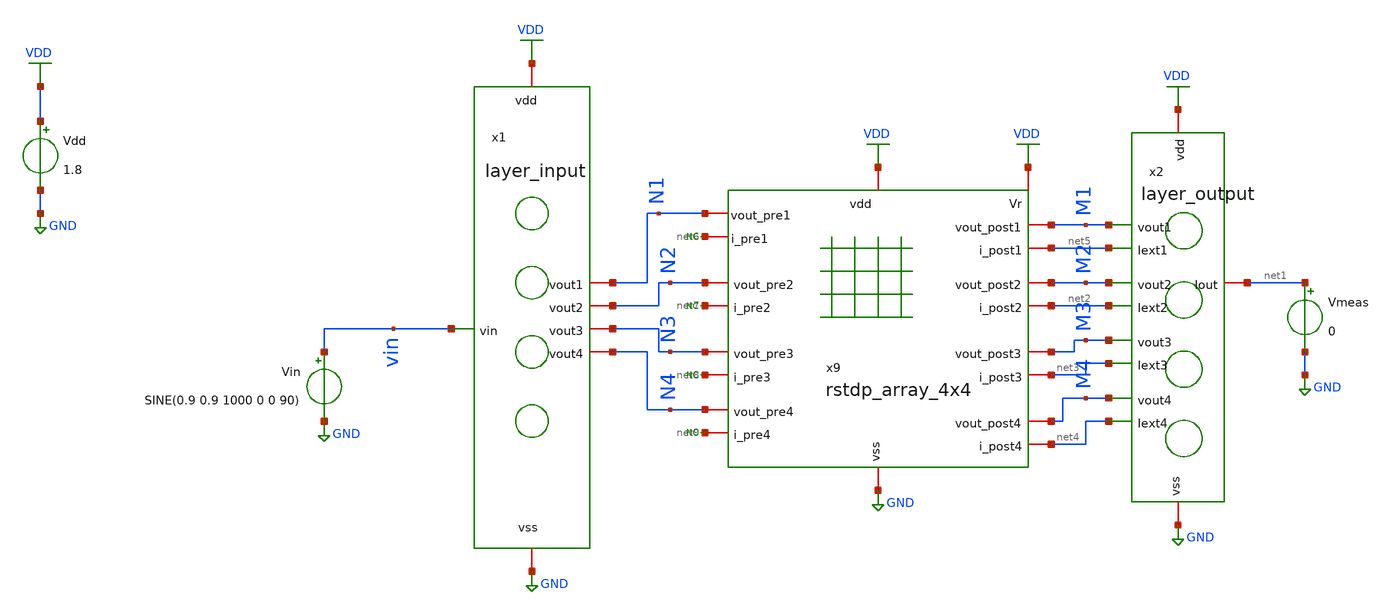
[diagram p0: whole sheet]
** sch_path: tb_4x4_modular.sch
**.subckt tb_4x4_modular
Vdd VDD GND 1.8
Vin vin GND SINE(0.9 0.9 1000 0 0 90)
x9 VDD VDD net2 net5 M2 net3 GND M1 M3 net4 M4 N1 net6 N2 net7 N3 net8 N4 net9 rstdp_array_4x4
Vmeas net1 GND 0
x1 VDD GND vin N1 N2 N3 N4 layer_input
x2 VDD net5 GND net2 net3 net1 net4 M1 M2 M3 M4 layer_output
* noconn #net6
* noconn #net7
* noconn #net8
* noconn #net9
**** begin user architecture code
.lib $::SKYWATER_MODELS/sky130.lib.spice tt

** opencircuitdesign pdks install
.inc $::SKYWATER_MODELS/rram_v0.spice
*.inc /home/alex/Desktop/EDA/SNN_IPN/memristor_models/wellposed/wllpsd.spice


**** end user architecture code
**.ends
.GLOBAL GND
.GLOBAL VDD
**** begin user architecture code


.option klu
.options num_threads=8
.tran 10u 100u uic
.control
	run
	write tb_4x4_modular.raw
.endc


**** end user architecture code
.end
